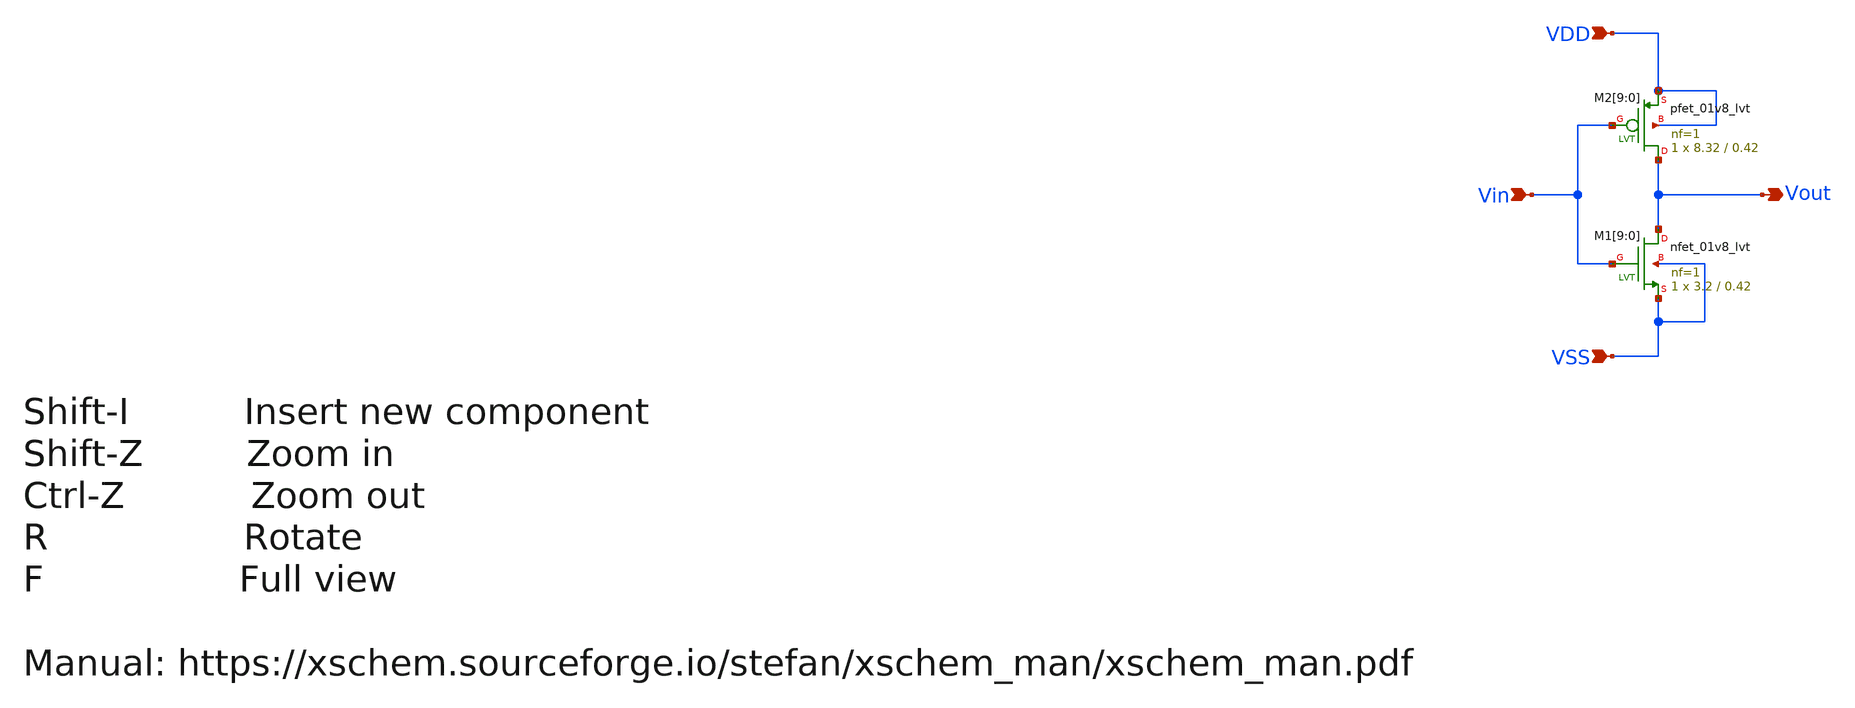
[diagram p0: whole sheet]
** sch_path: design/THESIS_EXP_RO_INVERTER_SKY130A/INV_LVT.sch
**.subckt INV_LVT VDD VSS Vin Vout
*.ipin VDD
*.ipin VSS
*.ipin Vin
*.opin Vout
XM1[9] Vout Vin VSS VSS sky130_fd_pr__nfet_01v8_lvt L=0.42 W=3.2 nf=1 ad='int((nf+1)/2) * W/nf * 0.29'
+ as='int((nf+2)/2) * W/nf * 0.29' pd='2*int((nf+1)/2) * (W/nf + 0.29)' ps='2*int((nf+2)/2) * (W/nf + 0.29)'
+ nrd='0.29 / W' nrs='0.29 / W' sa=0 sb=0 sd=0 mult=1 m=1
XM1[8] Vout Vin VSS VSS sky130_fd_pr__nfet_01v8_lvt L=0.42 W=3.2 nf=1 ad='int((nf+1)/2) * W/nf * 0.29'
+ as='int((nf+2)/2) * W/nf * 0.29' pd='2*int((nf+1)/2) * (W/nf + 0.29)' ps='2*int((nf+2)/2) * (W/nf + 0.29)'
+ nrd='0.29 / W' nrs='0.29 / W' sa=0 sb=0 sd=0 mult=1 m=1
XM1[7] Vout Vin VSS VSS sky130_fd_pr__nfet_01v8_lvt L=0.42 W=3.2 nf=1 ad='int((nf+1)/2) * W/nf * 0.29'
+ as='int((nf+2)/2) * W/nf * 0.29' pd='2*int((nf+1)/2) * (W/nf + 0.29)' ps='2*int((nf+2)/2) * (W/nf + 0.29)'
+ nrd='0.29 / W' nrs='0.29 / W' sa=0 sb=0 sd=0 mult=1 m=1
XM1[6] Vout Vin VSS VSS sky130_fd_pr__nfet_01v8_lvt L=0.42 W=3.2 nf=1 ad='int((nf+1)/2) * W/nf * 0.29'
+ as='int((nf+2)/2) * W/nf * 0.29' pd='2*int((nf+1)/2) * (W/nf + 0.29)' ps='2*int((nf+2)/2) * (W/nf + 0.29)'
+ nrd='0.29 / W' nrs='0.29 / W' sa=0 sb=0 sd=0 mult=1 m=1
XM1[5] Vout Vin VSS VSS sky130_fd_pr__nfet_01v8_lvt L=0.42 W=3.2 nf=1 ad='int((nf+1)/2) * W/nf * 0.29'
+ as='int((nf+2)/2) * W/nf * 0.29' pd='2*int((nf+1)/2) * (W/nf + 0.29)' ps='2*int((nf+2)/2) * (W/nf + 0.29)'
+ nrd='0.29 / W' nrs='0.29 / W' sa=0 sb=0 sd=0 mult=1 m=1
XM1[4] Vout Vin VSS VSS sky130_fd_pr__nfet_01v8_lvt L=0.42 W=3.2 nf=1 ad='int((nf+1)/2) * W/nf * 0.29'
+ as='int((nf+2)/2) * W/nf * 0.29' pd='2*int((nf+1)/2) * (W/nf + 0.29)' ps='2*int((nf+2)/2) * (W/nf + 0.29)'
+ nrd='0.29 / W' nrs='0.29 / W' sa=0 sb=0 sd=0 mult=1 m=1
XM1[3] Vout Vin VSS VSS sky130_fd_pr__nfet_01v8_lvt L=0.42 W=3.2 nf=1 ad='int((nf+1)/2) * W/nf * 0.29'
+ as='int((nf+2)/2) * W/nf * 0.29' pd='2*int((nf+1)/2) * (W/nf + 0.29)' ps='2*int((nf+2)/2) * (W/nf + 0.29)'
+ nrd='0.29 / W' nrs='0.29 / W' sa=0 sb=0 sd=0 mult=1 m=1
XM1[2] Vout Vin VSS VSS sky130_fd_pr__nfet_01v8_lvt L=0.42 W=3.2 nf=1 ad='int((nf+1)/2) * W/nf * 0.29'
+ as='int((nf+2)/2) * W/nf * 0.29' pd='2*int((nf+1)/2) * (W/nf + 0.29)' ps='2*int((nf+2)/2) * (W/nf + 0.29)'
+ nrd='0.29 / W' nrs='0.29 / W' sa=0 sb=0 sd=0 mult=1 m=1
XM1[1] Vout Vin VSS VSS sky130_fd_pr__nfet_01v8_lvt L=0.42 W=3.2 nf=1 ad='int((nf+1)/2) * W/nf * 0.29'
+ as='int((nf+2)/2) * W/nf * 0.29' pd='2*int((nf+1)/2) * (W/nf + 0.29)' ps='2*int((nf+2)/2) * (W/nf + 0.29)'
+ nrd='0.29 / W' nrs='0.29 / W' sa=0 sb=0 sd=0 mult=1 m=1
XM1[0] Vout Vin VSS VSS sky130_fd_pr__nfet_01v8_lvt L=0.42 W=3.2 nf=1 ad='int((nf+1)/2) * W/nf * 0.29'
+ as='int((nf+2)/2) * W/nf * 0.29' pd='2*int((nf+1)/2) * (W/nf + 0.29)' ps='2*int((nf+2)/2) * (W/nf + 0.29)'
+ nrd='0.29 / W' nrs='0.29 / W' sa=0 sb=0 sd=0 mult=1 m=1
XM2[9] Vout Vin VDD VDD sky130_fd_pr__pfet_01v8_lvt L=0.42 W=8.32 nf=1 ad='int((nf+1)/2) * W/nf * 0.29'
+ as='int((nf+2)/2) * W/nf * 0.29' pd='2*int((nf+1)/2) * (W/nf + 0.29)' ps='2*int((nf+2)/2) * (W/nf + 0.29)'
+ nrd='0.29 / W' nrs='0.29 / W' sa=0 sb=0 sd=0 mult=1 m=1
XM2[8] Vout Vin VDD VDD sky130_fd_pr__pfet_01v8_lvt L=0.42 W=8.32 nf=1 ad='int((nf+1)/2) * W/nf * 0.29'
+ as='int((nf+2)/2) * W/nf * 0.29' pd='2*int((nf+1)/2) * (W/nf + 0.29)' ps='2*int((nf+2)/2) * (W/nf + 0.29)'
+ nrd='0.29 / W' nrs='0.29 / W' sa=0 sb=0 sd=0 mult=1 m=1
XM2[7] Vout Vin VDD VDD sky130_fd_pr__pfet_01v8_lvt L=0.42 W=8.32 nf=1 ad='int((nf+1)/2) * W/nf * 0.29'
+ as='int((nf+2)/2) * W/nf * 0.29' pd='2*int((nf+1)/2) * (W/nf + 0.29)' ps='2*int((nf+2)/2) * (W/nf + 0.29)'
+ nrd='0.29 / W' nrs='0.29 / W' sa=0 sb=0 sd=0 mult=1 m=1
XM2[6] Vout Vin VDD VDD sky130_fd_pr__pfet_01v8_lvt L=0.42 W=8.32 nf=1 ad='int((nf+1)/2) * W/nf * 0.29'
+ as='int((nf+2)/2) * W/nf * 0.29' pd='2*int((nf+1)/2) * (W/nf + 0.29)' ps='2*int((nf+2)/2) * (W/nf + 0.29)'
+ nrd='0.29 / W' nrs='0.29 / W' sa=0 sb=0 sd=0 mult=1 m=1
XM2[5] Vout Vin VDD VDD sky130_fd_pr__pfet_01v8_lvt L=0.42 W=8.32 nf=1 ad='int((nf+1)/2) * W/nf * 0.29'
+ as='int((nf+2)/2) * W/nf * 0.29' pd='2*int((nf+1)/2) * (W/nf + 0.29)' ps='2*int((nf+2)/2) * (W/nf + 0.29)'
+ nrd='0.29 / W' nrs='0.29 / W' sa=0 sb=0 sd=0 mult=1 m=1
XM2[4] Vout Vin VDD VDD sky130_fd_pr__pfet_01v8_lvt L=0.42 W=8.32 nf=1 ad='int((nf+1)/2) * W/nf * 0.29'
+ as='int((nf+2)/2) * W/nf * 0.29' pd='2*int((nf+1)/2) * (W/nf + 0.29)' ps='2*int((nf+2)/2) * (W/nf + 0.29)'
+ nrd='0.29 / W' nrs='0.29 / W' sa=0 sb=0 sd=0 mult=1 m=1
XM2[3] Vout Vin VDD VDD sky130_fd_pr__pfet_01v8_lvt L=0.42 W=8.32 nf=1 ad='int((nf+1)/2) * W/nf * 0.29'
+ as='int((nf+2)/2) * W/nf * 0.29' pd='2*int((nf+1)/2) * (W/nf + 0.29)' ps='2*int((nf+2)/2) * (W/nf + 0.29)'
+ nrd='0.29 / W' nrs='0.29 / W' sa=0 sb=0 sd=0 mult=1 m=1
XM2[2] Vout Vin VDD VDD sky130_fd_pr__pfet_01v8_lvt L=0.42 W=8.32 nf=1 ad='int((nf+1)/2) * W/nf * 0.29'
+ as='int((nf+2)/2) * W/nf * 0.29' pd='2*int((nf+1)/2) * (W/nf + 0.29)' ps='2*int((nf+2)/2) * (W/nf + 0.29)'
+ nrd='0.29 / W' nrs='0.29 / W' sa=0 sb=0 sd=0 mult=1 m=1
XM2[1] Vout Vin VDD VDD sky130_fd_pr__pfet_01v8_lvt L=0.42 W=8.32 nf=1 ad='int((nf+1)/2) * W/nf * 0.29'
+ as='int((nf+2)/2) * W/nf * 0.29' pd='2*int((nf+1)/2) * (W/nf + 0.29)' ps='2*int((nf+2)/2) * (W/nf + 0.29)'
+ nrd='0.29 / W' nrs='0.29 / W' sa=0 sb=0 sd=0 mult=1 m=1
XM2[0] Vout Vin VDD VDD sky130_fd_pr__pfet_01v8_lvt L=0.42 W=8.32 nf=1 ad='int((nf+1)/2) * W/nf * 0.29'
+ as='int((nf+2)/2) * W/nf * 0.29' pd='2*int((nf+1)/2) * (W/nf + 0.29)' ps='2*int((nf+2)/2) * (W/nf + 0.29)'
+ nrd='0.29 / W' nrs='0.29 / W' sa=0 sb=0 sd=0 mult=1 m=1
**.ends
.end
